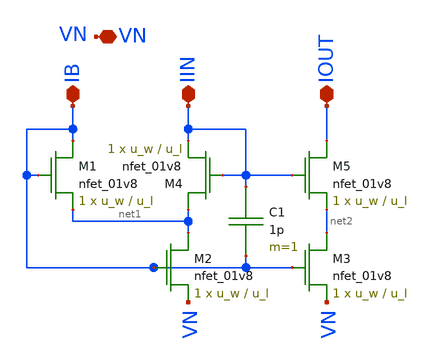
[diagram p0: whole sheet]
** sch_path: lib/analog/schematic/lvs_mirror.sch
**.subckt lvs_mirror VN IOUT IIN IB
*.iopin VN
*.iopin IOUT
*.iopin IIN
*.iopin IB
XM1 IB IB net1 GND sky130_fd_pr__nfet_01v8 L=u_l W=u_w nf=1 ad='int((nf+1)/2) * W/nf * 0.29' as='int((nf+2)/2) * W/nf * 0.29'
+ pd='2*int((nf+1)/2) * (W/nf + 0.29)' ps='2*int((nf+2)/2) * (W/nf + 0.29)' nrd='0.29 / W' nrs='0.29 / W'
+ sa=0 sb=0 sd=0 mult=1 m=1
XM2 net1 IB VN GND sky130_fd_pr__nfet_01v8 L=u_l W=u_w nf=1 ad='int((nf+1)/2) * W/nf * 0.29' as='int((nf+2)/2) * W/nf * 0.29'
+ pd='2*int((nf+1)/2) * (W/nf + 0.29)' ps='2*int((nf+2)/2) * (W/nf + 0.29)' nrd='0.29 / W' nrs='0.29 / W'
+ sa=0 sb=0 sd=0 mult=1 m=1
XM3 net2 IB VN GND sky130_fd_pr__nfet_01v8 L=u_l W=u_w nf=1 ad='int((nf+1)/2) * W/nf * 0.29' as='int((nf+2)/2) * W/nf * 0.29'
+ pd='2*int((nf+1)/2) * (W/nf + 0.29)' ps='2*int((nf+2)/2) * (W/nf + 0.29)' nrd='0.29 / W' nrs='0.29 / W'
+ sa=0 sb=0 sd=0 mult=1 m=1
XM4 net1 IIN IIN GND sky130_fd_pr__nfet_01v8 L=u_l W=u_w nf=1 ad='int((nf+1)/2) * W/nf * 0.29' as='int((nf+2)/2) * W/nf * 0.29'
+ pd='2*int((nf+1)/2) * (W/nf + 0.29)' ps='2*int((nf+2)/2) * (W/nf + 0.29)' nrd='0.29 / W' nrs='0.29 / W'
+ sa=0 sb=0 sd=0 mult=1 m=1
XM5 IOUT IIN net2 GND sky130_fd_pr__nfet_01v8 L=u_l W=u_w nf=1 ad='int((nf+1)/2) * W/nf * 0.29' as='int((nf+2)/2) * W/nf * 0.29'
+ pd='2*int((nf+1)/2) * (W/nf + 0.29)' ps='2*int((nf+2)/2) * (W/nf + 0.29)' nrd='0.29 / W' nrs='0.29 / W'
+ sa=0 sb=0 sd=0 mult=1 m=1
C1 IIN IB 1p m=1
**.ends
.end
